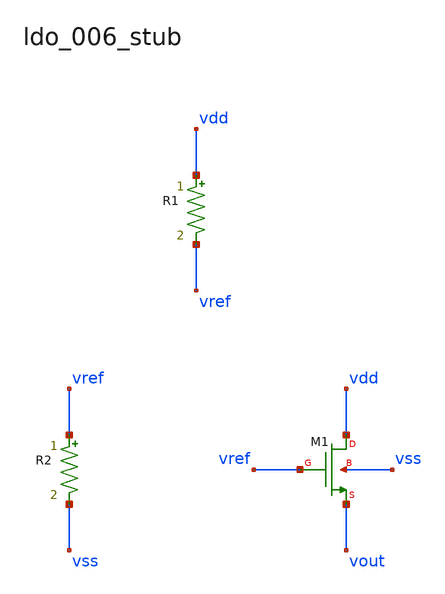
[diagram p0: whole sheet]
** sch_path: analog-db/raw/ldo_006_stub/hier/ldo_006_stub.sch
**.subckt ldo_006_stub
R1 vdd vref r_top m=1
R2 vref vss r_bot m=1
XM1 vdd vref vout vss sg13_lv_nmos w=x_dut_xm1_w l=x_dut_xm1_l ng=1 m=x_dut_xm1_m
**.ends
.end
